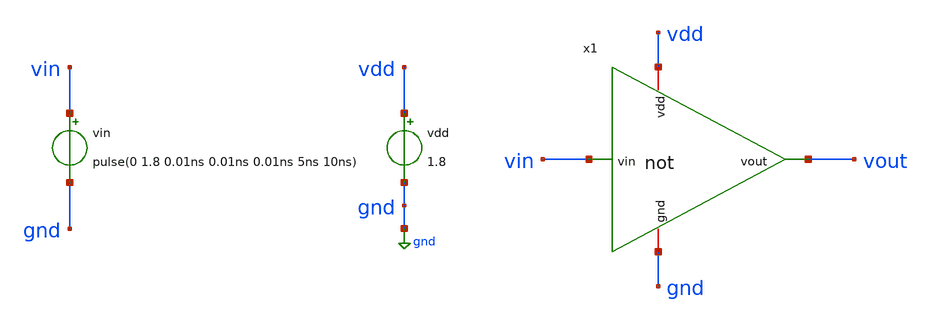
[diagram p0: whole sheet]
** sch_path: LogicGates/not_tb.sch
**.subckt not_tb
x1 vdd gnd vin vout not
vin vin gnd pulse(0 1.8 0.01ns 0.01ns 0.01ns 5ns 10ns)
vdd vdd gnd 1.8
**** begin user architecture code


.lib /usr/local/share/pdk/sky130A/libs.tech/ngspice/sky130.lib.spice tt
.control
    tran 0.1n 100n
    plot vin vout
.endc

.save all

**** end user architecture code
**.ends

* expanding   symbol:  LogicGates/not.sym # of pins=4
** sym_path: LogicGates/not.sym
** sch_path: LogicGates/not.sch
.subckt not vdd gnd vin vout
*.ipin vin
*.iopin vdd
*.iopin gnd
*.opin vout
XM2 vout vin vdd vdd sky130_fd_pr__pfet_01v8 L=0.15 W=2 nf=1 ad='int((nf+1)/2) * W/nf * 0.29' as='int((nf+2)/2) * W/nf * 0.29'
+ pd='2*int((nf+1)/2) * (W/nf + 0.29)' ps='2*int((nf+2)/2) * (W/nf + 0.29)' nrd='0.29 / W' nrs='0.29 / W'
+ sa=0 sb=0 sd=0 mult=1 m=1
XM1 vout vin gnd gnd sky130_fd_pr__nfet_01v8 L=0.15 W=1 nf=1 ad='int((nf+1)/2) * W/nf * 0.29' as='int((nf+2)/2) * W/nf * 0.29'
+ pd='2*int((nf+1)/2) * (W/nf + 0.29)' ps='2*int((nf+2)/2) * (W/nf + 0.29)' nrd='0.29 / W' nrs='0.29 / W'
+ sa=0 sb=0 sd=0 mult=1 m=1
.ends

.GLOBAL gnd
.end
